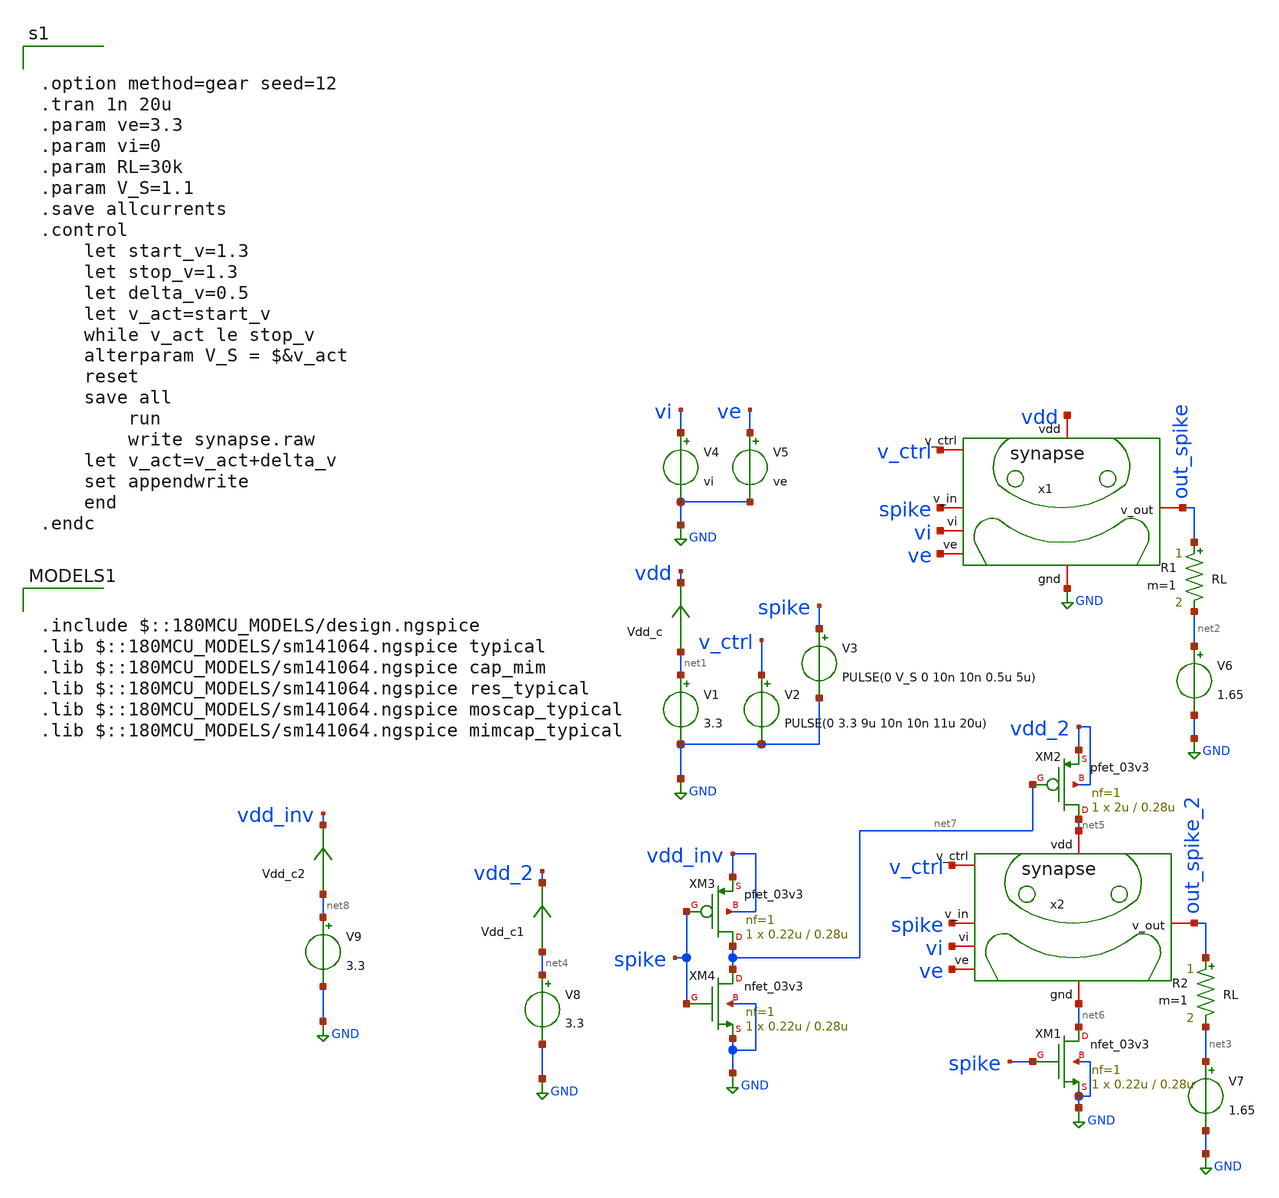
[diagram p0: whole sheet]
** sch_path: designs/libs/tb_synapse_pc/synapse_pc.sch
**.subckt synapse_pc
V1 net1 GND 3.3
Vdd_c net1 vdd 0
.save i(vdd_c)
V2 v_ctrl GND PULSE(0 3.3 9u 10n 10n 11u 20u)
V3 spike GND PULSE(0 V_S 0 10n 10n 0.5u 5u)
V4 vi GND vi
V5 ve GND ve
V6 net2 GND 1.65
R1 out_spike net2 RL m=1
x1 vdd spike ve v_ctrl out_spike vi GND synapse
V7 net3 GND 1.65
R2 out_spike_2 net3 RL m=1
x2 net5 spike ve v_ctrl out_spike_2 vi net6 synapse
V8 net4 GND 3.3
Vdd_c1 net4 vdd_2 0
.save i(vdd_c1)
XM1 net6 spike GND GND nfet_03v3 L=0.28u W=0.22u nf=1 ad='int((nf+1)/2) * W/nf * 0.18u' as='int((nf+2)/2) * W/nf * 0.18u'
+ pd='2*int((nf+1)/2) * (W/nf + 0.18u)' ps='2*int((nf+2)/2) * (W/nf + 0.18u)' nrd='0.18u / W' nrs='0.18u / W'
+ sa=0 sb=0 sd=0 m=1
XM2 net5 net7 vdd_2 vdd_2 pfet_03v3 L=0.28u W=2u nf=1 ad='int((nf+1)/2) * W/nf * 0.18u' as='int((nf+2)/2) * W/nf * 0.18u'
+ pd='2*int((nf+1)/2) * (W/nf + 0.18u)' ps='2*int((nf+2)/2) * (W/nf + 0.18u)' nrd='0.18u / W' nrs='0.18u / W'
+ sa=0 sb=0 sd=0 m=1
XM3 net7 spike vdd_inv vdd_inv pfet_03v3 L=0.28u W=0.22u nf=1 ad='int((nf+1)/2) * W/nf * 0.18u' as='int((nf+2)/2) * W/nf * 0.18u'
+ pd='2*int((nf+1)/2) * (W/nf + 0.18u)' ps='2*int((nf+2)/2) * (W/nf + 0.18u)' nrd='0.18u / W' nrs='0.18u / W'
+ sa=0 sb=0 sd=0 m=1
XM4 net7 spike GND GND nfet_03v3 L=0.28u W=0.22u nf=1 ad='int((nf+1)/2) * W/nf * 0.18u' as='int((nf+2)/2) * W/nf * 0.18u'
+ pd='2*int((nf+1)/2) * (W/nf + 0.18u)' ps='2*int((nf+2)/2) * (W/nf + 0.18u)' nrd='0.18u / W' nrs='0.18u / W'
+ sa=0 sb=0 sd=0 m=1
V9 net8 GND 3.3
Vdd_c2 net8 vdd_inv 0
.save i(vdd_c2)
**** begin user architecture code


.option method=gear seed=12
.tran 1n 20u
.param ve=3.3
.param vi=0
.param RL=30k
.param V_S=1.1
.save allcurrents
.control
    let start_v=1.3
    let stop_v=1.3
    let delta_v=0.5
    let v_act=start_v
    while v_act le stop_v
	alterparam V_S = $&v_act
	reset
	save all
        run
        write synapse.raw
	let v_act=v_act+delta_v
	set appendwrite
    end
.endc



.include $::180MCU_MODELS/design.ngspice
.lib $::180MCU_MODELS/sm141064.ngspice typical
.lib $::180MCU_MODELS/sm141064.ngspice cap_mim
.lib $::180MCU_MODELS/sm141064.ngspice res_typical
.lib $::180MCU_MODELS/sm141064.ngspice moscap_typical
.lib $::180MCU_MODELS/sm141064.ngspice mimcap_typical

**** end user architecture code
**.ends

* expanding   symbol:  designs/libs/core_synapse/synapse.sym # of pins=7
** sym_path: designs/libs/core_synapse/synapse.sym
** sch_path: designs/libs/core_synapse/synapse.sch
.subckt synapse vdd v_in ve v_ctrl v_out vi gnd
*.iopin v_out
*.iopin v_ctrl
*.iopin ve
*.iopin vi
*.iopin v_in
*.iopin vdd
*.iopin gnd
XM5 net2 net2 vdd vdd pfet_03v3 L=0.28u W=0.22u nf=1 ad='int((nf+1)/2) * W/nf * 0.18u' as='int((nf+2)/2) * W/nf * 0.18u'
+ pd='2*int((nf+1)/2) * (W/nf + 0.18u)' ps='2*int((nf+2)/2) * (W/nf + 0.18u)' nrd='0.18u / W' nrs='0.18u / W'
+ sa=0 sb=0 sd=0 m=1
XM1 net1 v_in vdd vdd pfet_03v3 L=0.28u W=0.22u nf=1 ad='int((nf+1)/2) * W/nf * 0.18u' as='int((nf+2)/2) * W/nf * 0.18u'
+ pd='2*int((nf+1)/2) * (W/nf + 0.18u)' ps='2*int((nf+2)/2) * (W/nf + 0.18u)' nrd='0.18u / W' nrs='0.18u / W'
+ sa=0 sb=0 sd=0 m=1
XM3 net1 v_in gnd gnd nfet_03v3 L=0.28u W=0.22u nf=1 ad='int((nf+1)/2) * W/nf * 0.18u' as='int((nf+2)/2) * W/nf * 0.18u'
+ pd='2*int((nf+1)/2) * (W/nf + 0.18u)' ps='2*int((nf+2)/2) * (W/nf + 0.18u)' nrd='0.18u / W' nrs='0.18u / W'
+ sa=0 sb=0 sd=0 m=1
XM4 net2 v_in net3 gnd nfet_03v3 L=0.28u W=0.22u nf=1 ad='int((nf+1)/2) * W/nf * 0.18u' as='int((nf+2)/2) * W/nf * 0.18u'
+ pd='2*int((nf+1)/2) * (W/nf + 0.18u)' ps='2*int((nf+2)/2) * (W/nf + 0.18u)' nrd='0.18u / W' nrs='0.18u / W'
+ sa=0 sb=0 sd=0 m=1
XM6 net3 ve gnd gnd nfet_03v3 L=0.28u W=0.22u nf=1 ad='int((nf+1)/2) * W/nf * 0.18u' as='int((nf+2)/2) * W/nf * 0.18u'
+ pd='2*int((nf+1)/2) * (W/nf + 0.18u)' ps='2*int((nf+2)/2) * (W/nf + 0.18u)' nrd='0.18u / W' nrs='0.18u / W'
+ sa=0 sb=0 sd=0 m=1
XM7 net5 vi vdd vdd pfet_03v3 L=0.28u W=0.22u nf=1 ad='int((nf+1)/2) * W/nf * 0.18u' as='int((nf+2)/2) * W/nf * 0.18u'
+ pd='2*int((nf+1)/2) * (W/nf + 0.18u)' ps='2*int((nf+2)/2) * (W/nf + 0.18u)' nrd='0.18u / W' nrs='0.18u / W'
+ sa=0 sb=0 sd=0 m=1
XM8 net4 net1 net5 vdd pfet_03v3 L=0.28u W=0.22u nf=1 ad='int((nf+1)/2) * W/nf * 0.18u' as='int((nf+2)/2) * W/nf * 0.18u'
+ pd='2*int((nf+1)/2) * (W/nf + 0.18u)' ps='2*int((nf+2)/2) * (W/nf + 0.18u)' nrd='0.18u / W' nrs='0.18u / W'
+ sa=0 sb=0 sd=0 m=1
XM9 net4 net4 gnd gnd nfet_03v3 L=0.28u W=0.22u nf=1 ad='int((nf+1)/2) * W/nf * 0.18u' as='int((nf+2)/2) * W/nf * 0.18u'
+ pd='2*int((nf+1)/2) * (W/nf + 0.18u)' ps='2*int((nf+2)/2) * (W/nf + 0.18u)' nrd='0.18u / W' nrs='0.18u / W'
+ sa=0 sb=0 sd=0 m=1
XM2 net7 net2 vdd vdd pfet_03v3 L=0.28u W=2.8u nf=1 ad='int((nf+1)/2) * W/nf * 0.18u' as='int((nf+2)/2) * W/nf * 0.18u'
+ pd='2*int((nf+1)/2) * (W/nf + 0.18u)' ps='2*int((nf+2)/2) * (W/nf + 0.18u)' nrd='0.18u / W' nrs='0.18u / W'
+ sa=0 sb=0 sd=0 m=1
XM10 v_out v_ctrl net7 vdd pfet_03v3 L=0.28u W=2.8u nf=1 ad='int((nf+1)/2) * W/nf * 0.18u' as='int((nf+2)/2) * W/nf * 0.18u'
+ pd='2*int((nf+1)/2) * (W/nf + 0.18u)' ps='2*int((nf+2)/2) * (W/nf + 0.18u)' nrd='0.18u / W' nrs='0.18u / W'
+ sa=0 sb=0 sd=0 m=1
XM11 v_out v_ctrl net6 gnd nfet_03v3 L=0.28u W=2u nf=1 ad='int((nf+1)/2) * W/nf * 0.18u' as='int((nf+2)/2) * W/nf * 0.18u'
+ pd='2*int((nf+1)/2) * (W/nf + 0.18u)' ps='2*int((nf+2)/2) * (W/nf + 0.18u)' nrd='0.18u / W' nrs='0.18u / W'
+ sa=0 sb=0 sd=0 m=1
XM12 net6 net4 gnd gnd nfet_03v3 L=0.28u W=1u nf=1 ad='int((nf+1)/2) * W/nf * 0.18u' as='int((nf+2)/2) * W/nf * 0.18u'
+ pd='2*int((nf+1)/2) * (W/nf + 0.18u)' ps='2*int((nf+2)/2) * (W/nf + 0.18u)' nrd='0.18u / W' nrs='0.18u / W'
+ sa=0 sb=0 sd=0 m=1
.ends

.GLOBAL GND
.end
